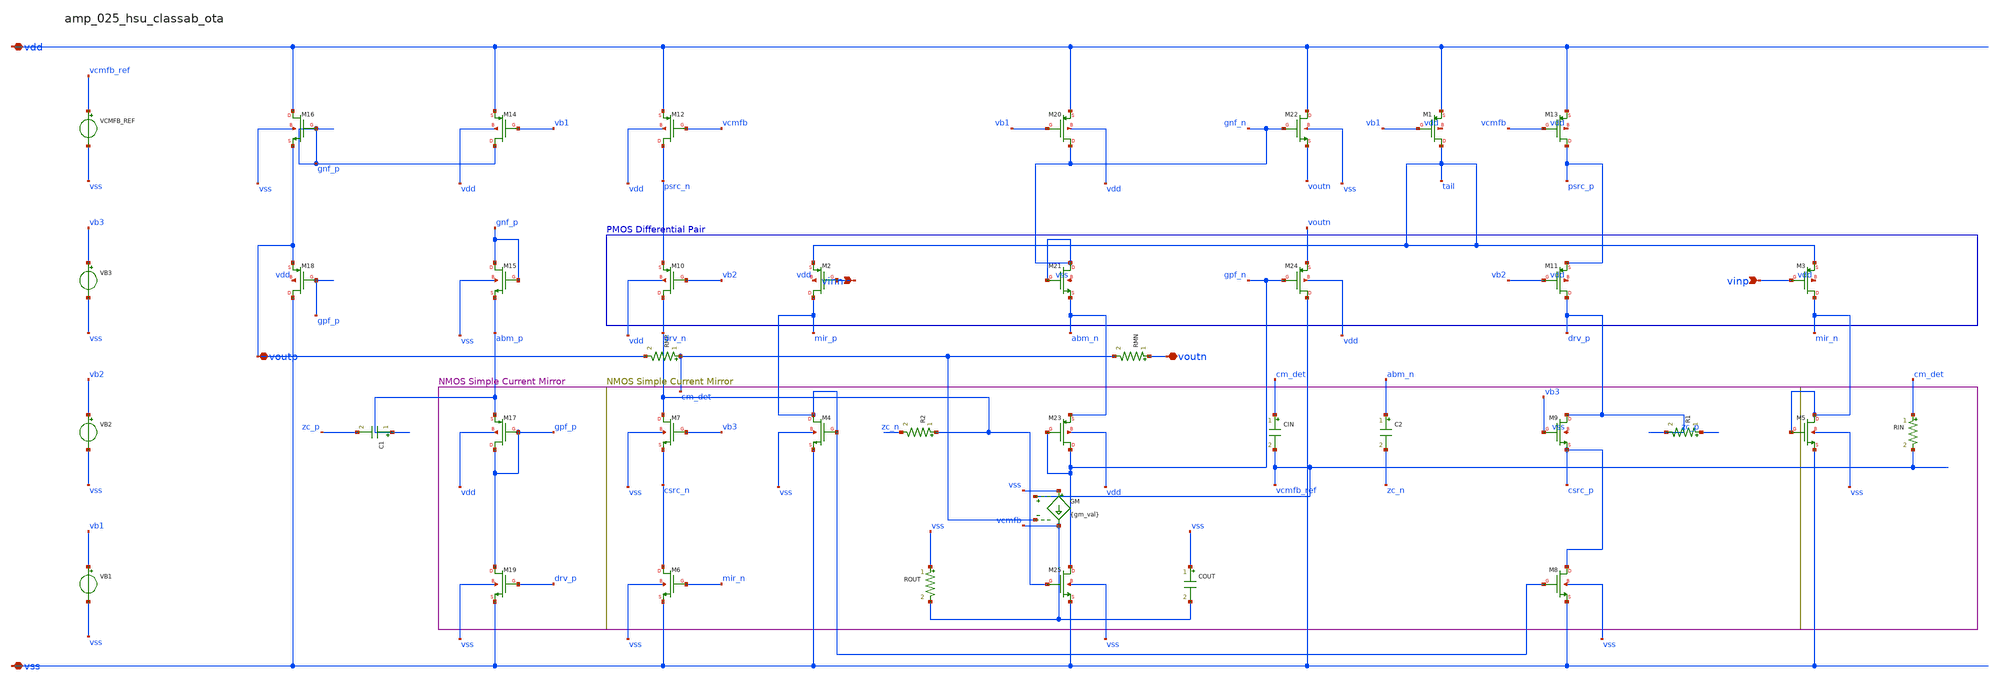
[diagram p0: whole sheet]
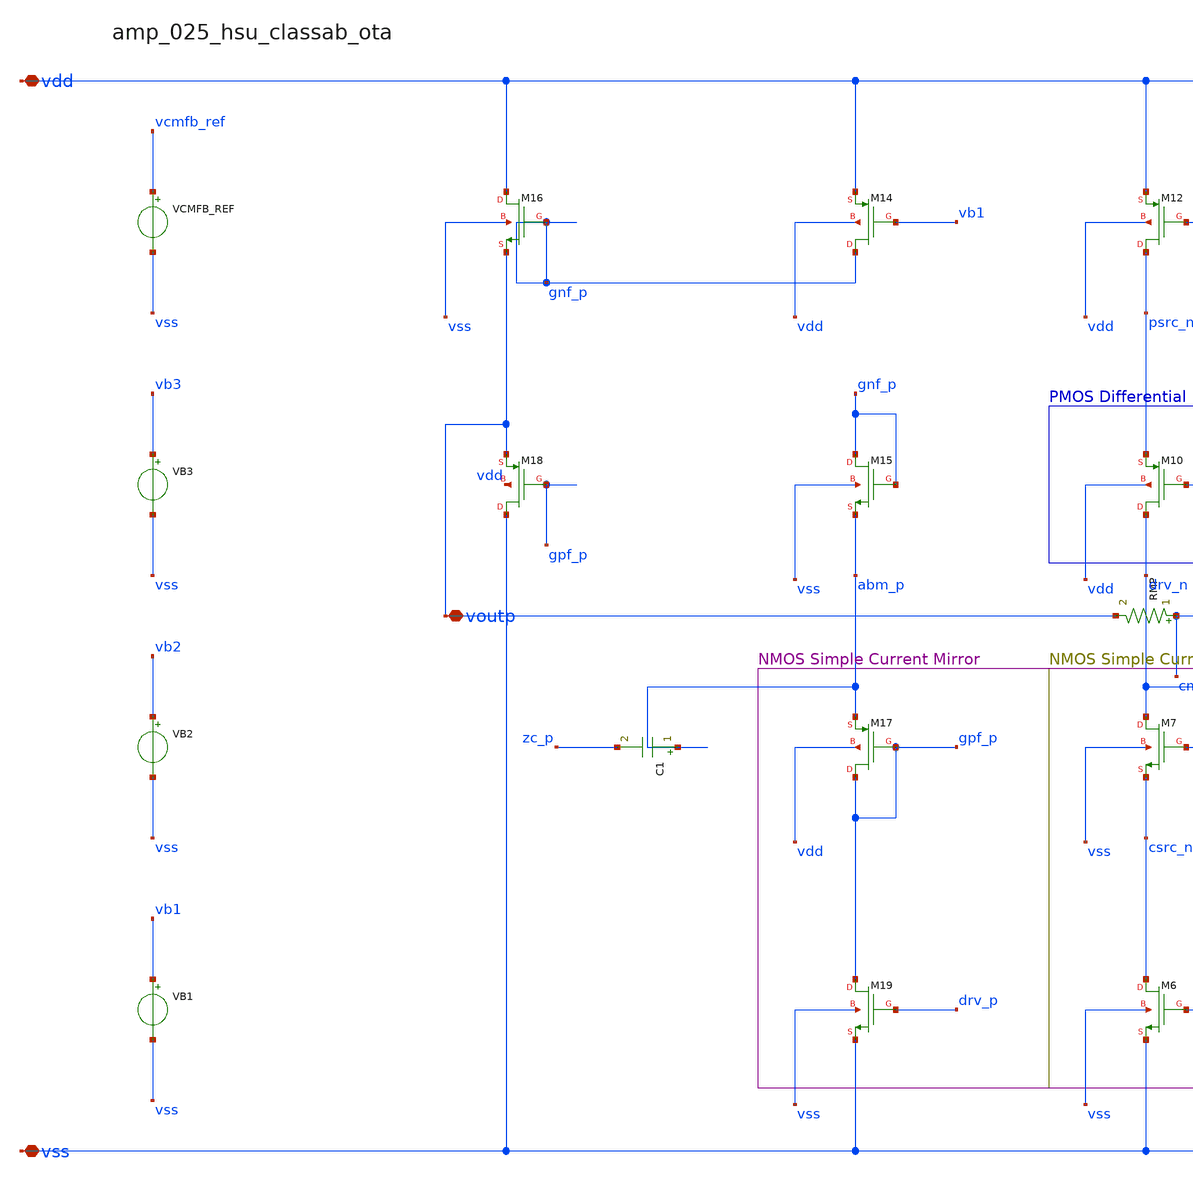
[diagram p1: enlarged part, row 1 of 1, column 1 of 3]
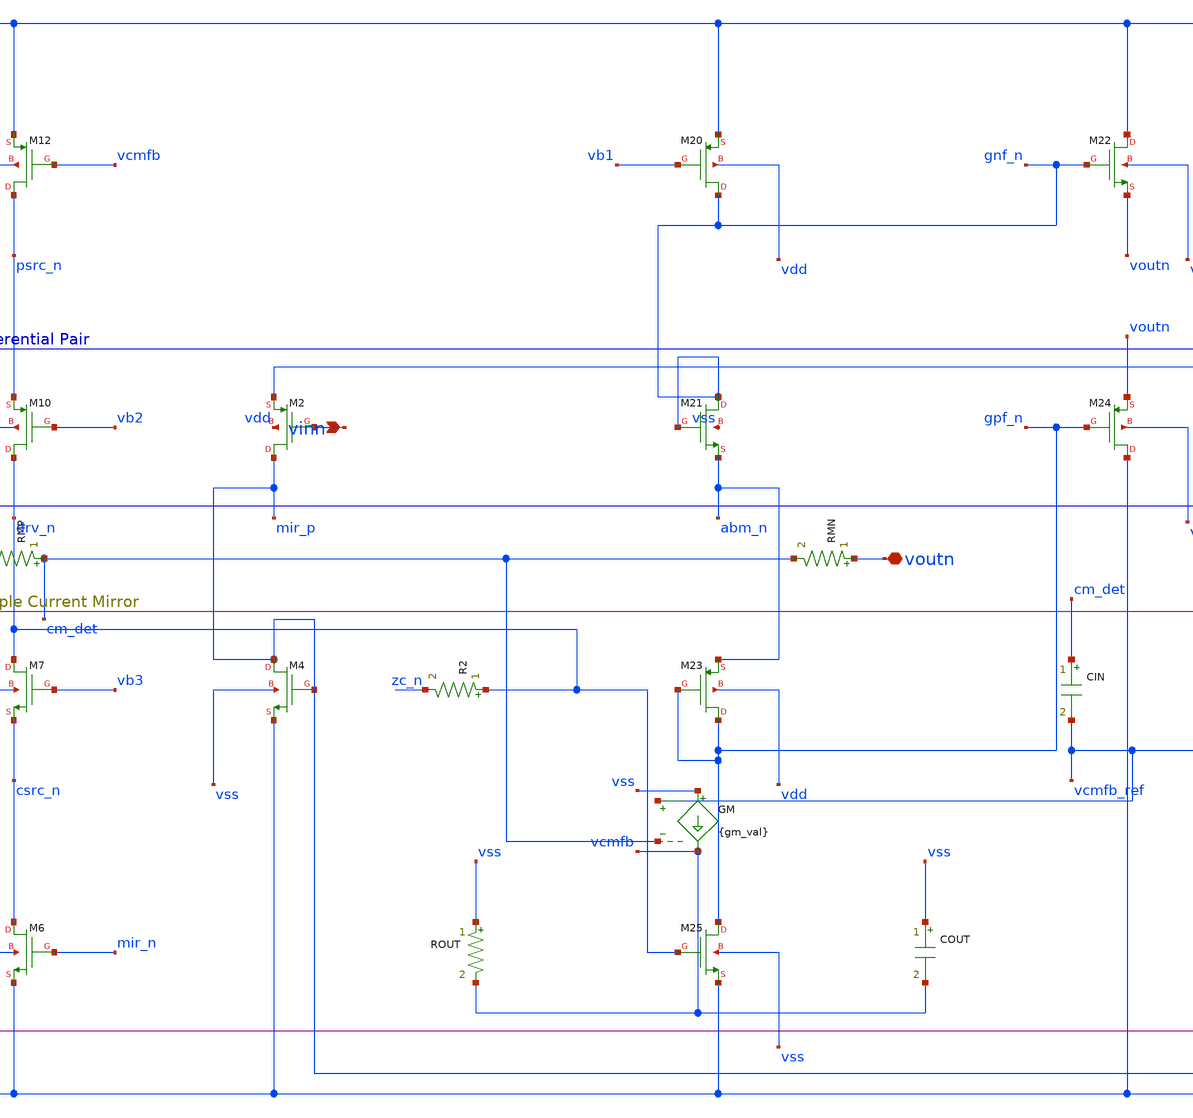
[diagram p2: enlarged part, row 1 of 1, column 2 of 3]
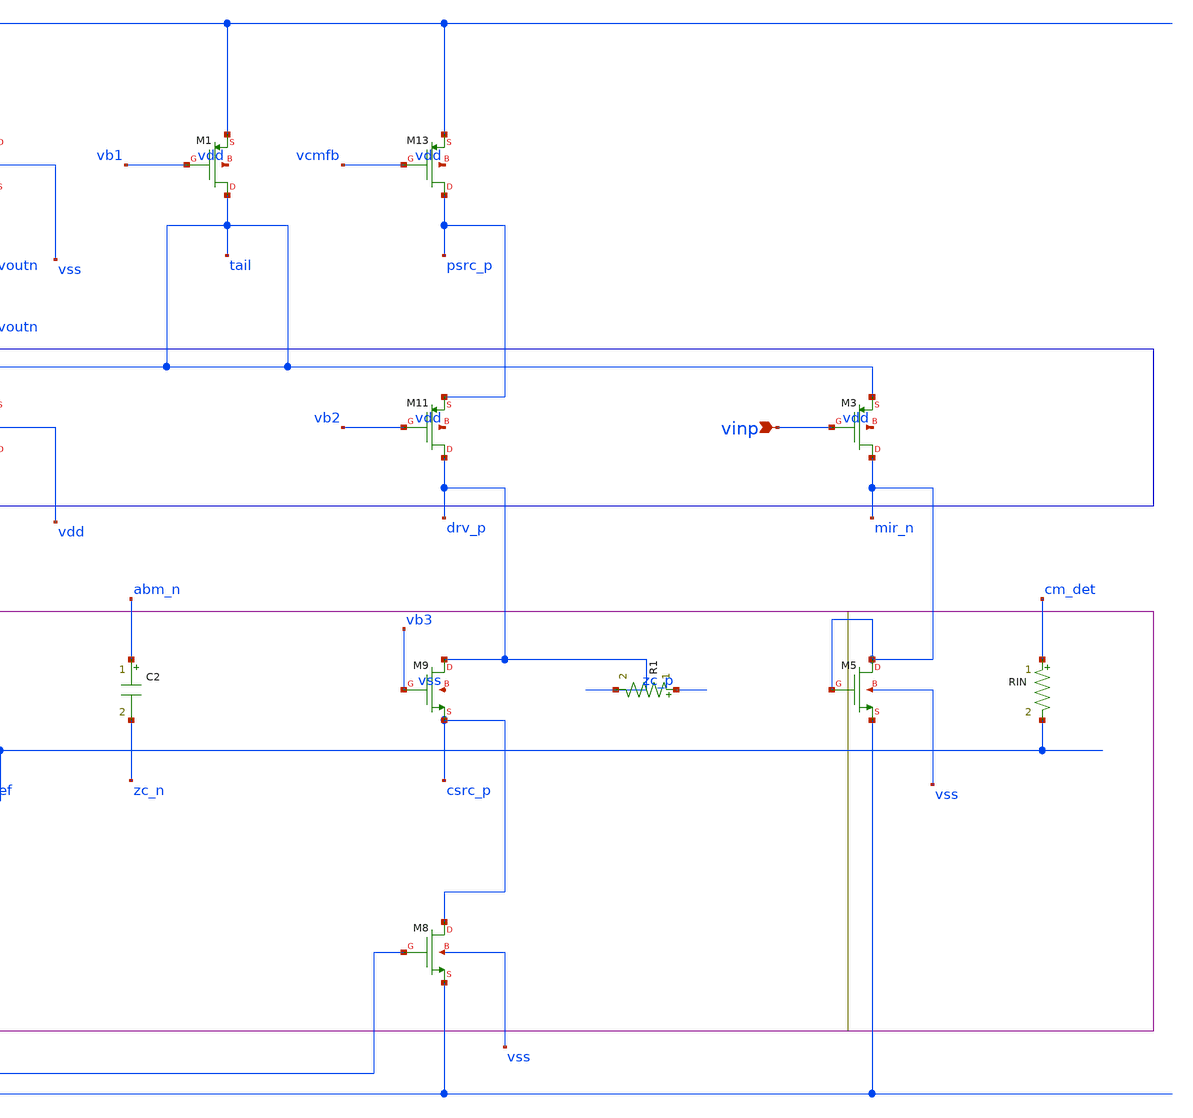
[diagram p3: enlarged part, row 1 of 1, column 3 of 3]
** sch_path: analog-db/raw/amp_025_hsu_classab_ota/amp_025_hsu_classab_ota_annotated.sch
**.subckt amp_025_hsu_classab_ota_annotated vinn vinp vdd vss voutp voutn
*.ipin vinn
*.ipin vinp
*.iopin vdd
*.iopin vss
*.iopin voutp
*.iopin voutn
C1 abm_p zc_p 'x_dut_c1_value' m=1
C2 abm_n zc_n 'x_dut_c2_value' m=1
CIN cm_det vcmfb_ref 'cin_val' m=1
COUT vss vcmfb 'cout_val' m=1
GM vss vcmfb vcmfb_ref cm_det {gm_val}
R1 zc_p drv_p 'x_dut_r1_value' m=1
R2 drv_n zc_n 'x_dut_r2_value' m=1
RIN cm_det vcmfb_ref 'rin_val' m=1
RMN voutn cm_det 'x_dut_rmn_value' m=1
RMP cm_det voutp 'x_dut_rmp_value' m=1
ROUT vss vcmfb 'rout_val' m=1
VB1 vb1 vss dc {vb1}
VB2 vb2 vss dc {vb2}
VB3 vb3 vss dc {vb3}
VCMFB_REF vcmfb_ref vss dc {vcmfb_ref}
XM1 tail vb1 vdd vdd sg13_lv_pmos w=x_dut_xm1_w l=x_dut_xm1_l ng=1 m=x_dut_xm1_m
XM10 drv_n vb2 psrc_n vdd sg13_lv_pmos w=x_dut_xm10_w l=x_dut_xm10_l ng=1 m=x_dut_xm10_m
XM11 drv_p vb2 psrc_p vdd sg13_lv_pmos w=x_dut_xm11_w l=x_dut_xm11_l ng=1 m=x_dut_xm11_m
XM12 psrc_n vcmfb vdd vdd sg13_lv_pmos w=x_dut_xm12_w l=x_dut_xm12_l ng=1 m=x_dut_xm12_m
XM13 psrc_p vcmfb vdd vdd sg13_lv_pmos w=x_dut_xm13_w l=x_dut_xm13_l ng=1 m=x_dut_xm13_m
XM14 gnf_p vb1 vdd vdd sg13_lv_pmos w=x_dut_xm14_w l=x_dut_xm14_l ng=1 m=x_dut_xm14_m
XM15 gnf_p gnf_p abm_p vss sg13_lv_nmos w=x_dut_xm15_w l=x_dut_xm15_l ng=1 m=x_dut_xm15_m
XM16 vdd gnf_p voutp vss sg13_lv_nmos w=x_dut_xm16_w l=x_dut_xm16_l ng=1 m=x_dut_xm16_m
XM17 gpf_p gpf_p abm_p vdd sg13_lv_pmos w=x_dut_xm17_w l=x_dut_xm17_l ng=1 m=x_dut_xm17_m
XM18 vss gpf_p voutp vdd sg13_lv_pmos w=x_dut_xm18_w l=x_dut_xm18_l ng=1 m=x_dut_xm18_m
XM19 gpf_p drv_p vss vss sg13_lv_nmos w=x_dut_xm19_w l=x_dut_xm19_l ng=1 m=x_dut_xm19_m
XM2 mir_p vinn tail vdd sg13_lv_pmos w=x_dut_xm2_w l=x_dut_xm2_l ng=1 m=x_dut_xm2_m
XM20 gnf_n vb1 vdd vdd sg13_lv_pmos w=x_dut_xm20_w l=x_dut_xm20_l ng=1 m=x_dut_xm20_m
XM21 gnf_n gnf_n abm_n vss sg13_lv_nmos w=x_dut_xm21_w l=x_dut_xm21_l ng=1 m=x_dut_xm21_m
XM22 vdd gnf_n voutn vss sg13_lv_nmos w=x_dut_xm22_w l=x_dut_xm22_l ng=1 m=x_dut_xm22_m
XM23 gpf_n gpf_n abm_n vdd sg13_lv_pmos w=x_dut_xm23_w l=x_dut_xm23_l ng=1 m=x_dut_xm23_m
XM24 vss gpf_n voutn vdd sg13_lv_pmos w=x_dut_xm24_w l=x_dut_xm24_l ng=1 m=x_dut_xm24_m
XM25 gpf_n drv_n vss vss sg13_lv_nmos w=x_dut_xm25_w l=x_dut_xm25_l ng=1 m=x_dut_xm25_m
XM3 mir_n vinp tail vdd sg13_lv_pmos w=x_dut_xm3_w l=x_dut_xm3_l ng=1 m=x_dut_xm3_m
XM4 mir_p mir_p vss vss sg13_lv_nmos w=x_dut_xm4_w l=x_dut_xm4_l ng=1 m=x_dut_xm4_m
XM5 mir_n mir_n vss vss sg13_lv_nmos w=x_dut_xm5_w l=x_dut_xm5_l ng=1 m=x_dut_xm5_m
XM6 csrc_n mir_n vss vss sg13_lv_nmos w=x_dut_xm6_w l=x_dut_xm6_l ng=1 m=x_dut_xm6_m
XM7 drv_n vb3 csrc_n vss sg13_lv_nmos w=x_dut_xm7_w l=x_dut_xm7_l ng=1 m=x_dut_xm7_m
XM8 csrc_p mir_p vss vss sg13_lv_nmos w=x_dut_xm8_w l=x_dut_xm8_l ng=1 m=x_dut_xm8_m
XM9 drv_p vb3 csrc_p vss sg13_lv_nmos w=x_dut_xm9_w l=x_dut_xm9_l ng=1 m=x_dut_xm9_m
**.ends
.end
